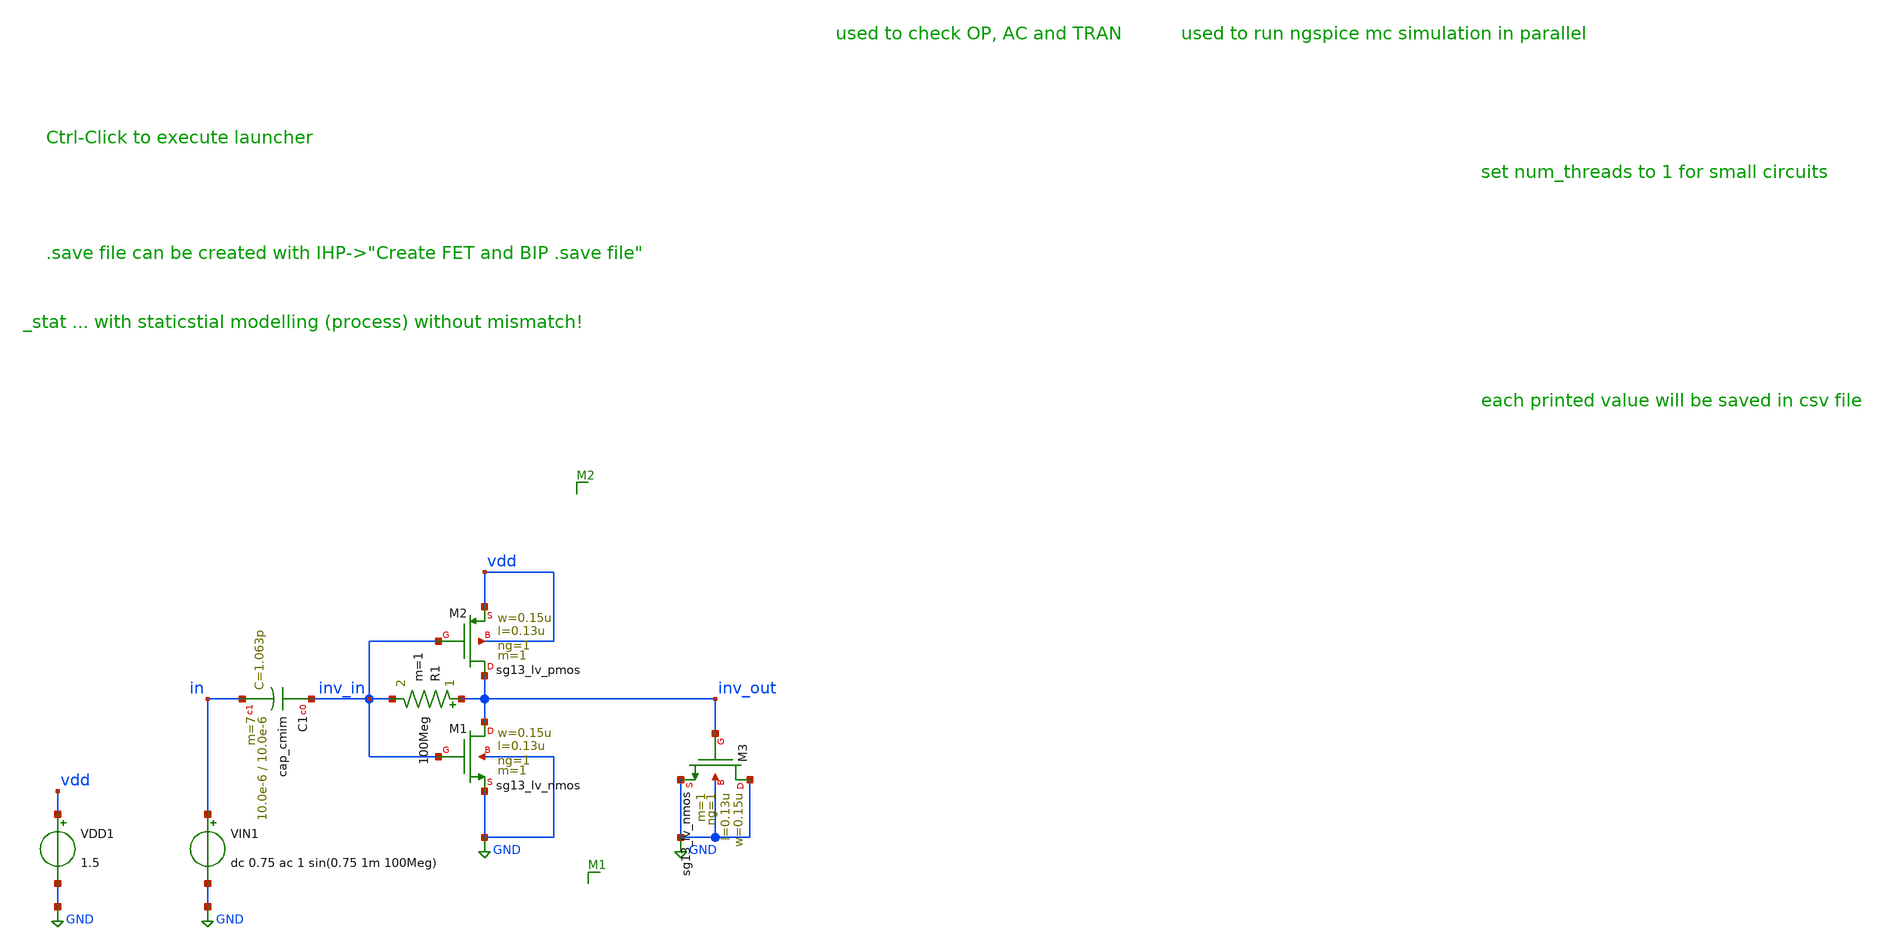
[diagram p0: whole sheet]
** sch_path: ihp-sg13g2/xschem_libs/sg13g2_tests_ase/inv_mc_tb/schematic/inv_mc_tb.sch
**.subckt inv_mc_tb
VDD1 vdd GND 1.5
XM1 inv_out inv_in GND GND sg13_lv_nmos w=0.15u l=0.13u ng=1 m=1 mm_ok=1
XM2 inv_out inv_in vdd vdd sg13_lv_pmos w=0.15u l=0.13u ng=1 m=1 mm_ok=1
XM3 GND inv_out GND GND sg13_lv_nmos w=0.15u l=0.13u ng=1 m=1 mm_ok=1
VIN1 in GND dc 0.75 ac 1 sin(0.75 1m 100Meg)
R1 inv_out inv_in 100Meg m=1
XC1 inv_in in cap_cmim w=10.0e-6 l=10.0e-6 m=7 mm_ok=1
**.ends
.GLOBAL GND
.end
